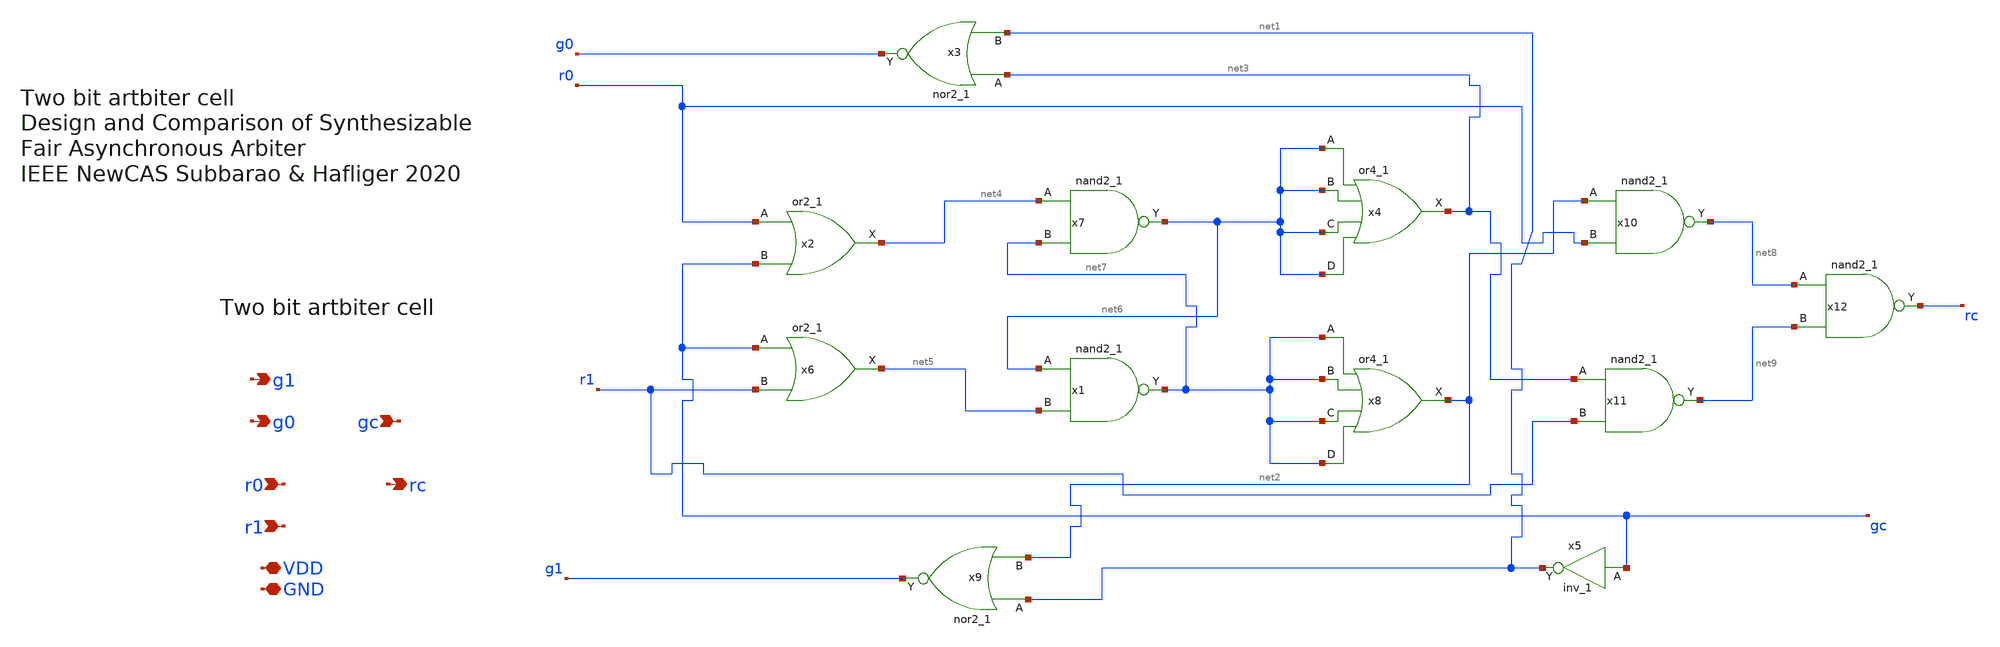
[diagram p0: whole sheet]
** sch_path: design/xschem/arbiter_cell_two_bits_fc_v1.sch
**.subckt arbiter_cell_two_bits_fc_v1 r1 r0 g0 g1 rc gc GND VDD
*.ipin r1
*.ipin r0
*.opin g0
*.opin g1
*.opin rc
*.ipin gc
*.iopin GND
*.iopin VDD
x1 net6 net5 GND GND VDD VDD net7 sky130_fd_sc_hd__nand2_1
x2 r0 gc GND GND VDD VDD net4 sky130_fd_sc_hd__or2_1
x3 net3 net1 GND GND VDD VDD g0 sky130_fd_sc_hd__nor2_1
x4 net6 net6 net6 net6 GND GND VDD VDD net3 sky130_fd_sc_hd__or4_1
x5 gc GND GND VDD VDD net1 sky130_fd_sc_hd__inv_1
x6 gc r1 GND GND VDD VDD net5 sky130_fd_sc_hd__or2_1
x7 net4 net7 GND GND VDD VDD net6 sky130_fd_sc_hd__nand2_1
x8 net7 net7 net7 net7 GND GND VDD VDD net2 sky130_fd_sc_hd__or4_1
x9 net1 net2 GND GND VDD VDD g1 sky130_fd_sc_hd__nor2_1
x10 net2 r0 GND GND VDD VDD net8 sky130_fd_sc_hd__nand2_1
x11 net3 r1 GND GND VDD VDD net9 sky130_fd_sc_hd__nand2_1
x12 net8 net9 GND GND VDD VDD rc sky130_fd_sc_hd__nand2_1
**.ends
.end
